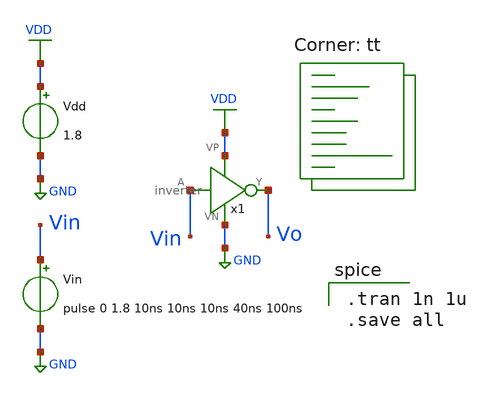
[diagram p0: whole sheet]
** sch_path: week 0/simpre-layout/inverter_tran_test.sch
**.subckt inverter_tran_test
x1 Vin VDD Vo GND inverter
Vdd VDD GND 1.8
Vin Vin GND pulse 0 1.8 10ns 10ns 10ns 40ns 100ns
**** begin user architecture code

.tran 1n 1u
.save all

 .lib /usr/local/share/pdk/sky130A/libs.tech/ngspice/sky130.lib.spice tt
**** end user architecture code
**.ends
.GLOBAL VDD
.GLOBAL GND
.end
